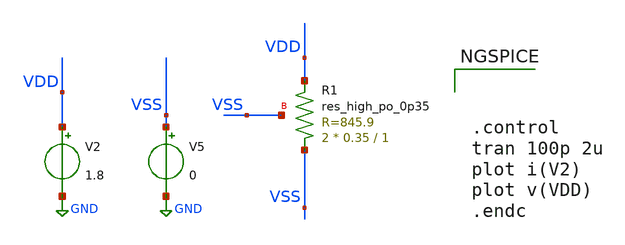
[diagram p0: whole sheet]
** sch_path: xschem/DC_DC_Converter_xschem/OTHERS/resistor_check.sch
**.subckt resistor_check
XR1 VSS VDD VSS sky130_fd_pr__res_high_po_0p35 L=1 mult=2 m=2
V2 VDD GND 1.8
V5 VSS GND 0
**** begin user architecture code

** opencircuitdesign pdks install
.lib $::SKYWATER_MODELS/sky130.lib.spice tt





.control
tran 100p 2u
plot i(V2)
plot v(VDD)
.endc


**** end user architecture code
**.ends
.GLOBAL GND
.end
